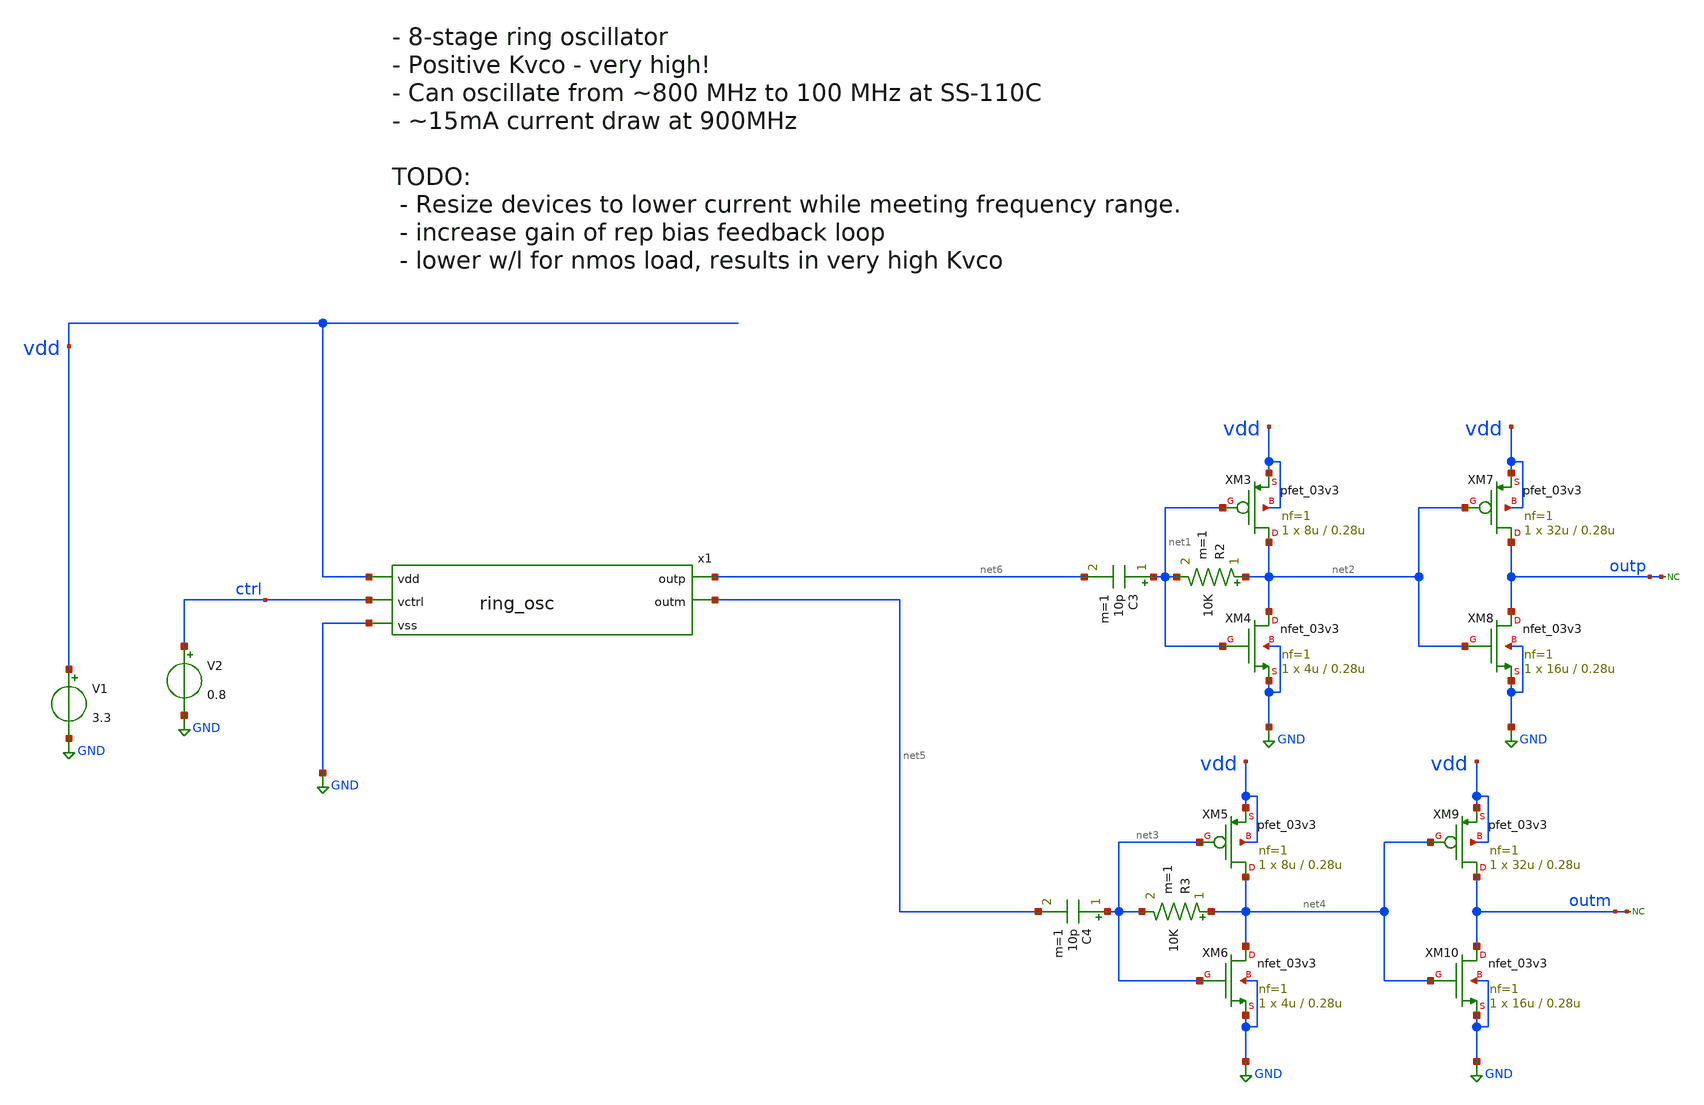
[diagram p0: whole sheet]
** sch_path: xschem/tb_ring_osc_p.sch
**.subckt tb_ring_osc_p
V1 vdd GND 3.3
x1 net6 net5 vdd ctrl GND ring_osc
V2 ctrl GND 0.8
XM3 net2 net1 vdd vdd pfet_03v3 L=0.28u W=8u nf=1 ad='int((nf+1)/2) * W/nf * 0.18u' as='int((nf+2)/2) * W/nf * 0.18u'
+ pd='2*int((nf+1)/2) * (W/nf + 0.18u)' ps='2*int((nf+2)/2) * (W/nf + 0.18u)' nrd='0.18u / W' nrs='0.18u / W'
+ sa=0 sb=0 sd=0 m=1
XM4 net2 net1 GND GND nfet_03v3 L=0.28u W=4u nf=1 ad='int((nf+1)/2) * W/nf * 0.18u' as='int((nf+2)/2) * W/nf * 0.18u'
+ pd='2*int((nf+1)/2) * (W/nf + 0.18u)' ps='2*int((nf+2)/2) * (W/nf + 0.18u)' nrd='0.18u / W' nrs='0.18u / W'
+ sa=0 sb=0 sd=0 m=1
R2 net2 net1 10K m=1
C3 net1 net6 10p m=1
XM5 net4 net3 vdd vdd pfet_03v3 L=0.28u W=8u nf=1 ad='int((nf+1)/2) * W/nf * 0.18u' as='int((nf+2)/2) * W/nf * 0.18u'
+ pd='2*int((nf+1)/2) * (W/nf + 0.18u)' ps='2*int((nf+2)/2) * (W/nf + 0.18u)' nrd='0.18u / W' nrs='0.18u / W'
+ sa=0 sb=0 sd=0 m=1
XM6 net4 net3 GND GND nfet_03v3 L=0.28u W=4u nf=1 ad='int((nf+1)/2) * W/nf * 0.18u' as='int((nf+2)/2) * W/nf * 0.18u'
+ pd='2*int((nf+1)/2) * (W/nf + 0.18u)' ps='2*int((nf+2)/2) * (W/nf + 0.18u)' nrd='0.18u / W' nrs='0.18u / W'
+ sa=0 sb=0 sd=0 m=1
R3 net4 net3 10K m=1
C4 net3 net5 10p m=1
* noconn outp
XM7 outp net2 vdd vdd pfet_03v3 L=0.28u W=32u nf=1 ad='int((nf+1)/2) * W/nf * 0.18u' as='int((nf+2)/2) * W/nf * 0.18u'
+ pd='2*int((nf+1)/2) * (W/nf + 0.18u)' ps='2*int((nf+2)/2) * (W/nf + 0.18u)' nrd='0.18u / W' nrs='0.18u / W'
+ sa=0 sb=0 sd=0 m=1
XM8 outp net2 GND GND nfet_03v3 L=0.28u W=16u nf=1 ad='int((nf+1)/2) * W/nf * 0.18u' as='int((nf+2)/2) * W/nf * 0.18u'
+ pd='2*int((nf+1)/2) * (W/nf + 0.18u)' ps='2*int((nf+2)/2) * (W/nf + 0.18u)' nrd='0.18u / W' nrs='0.18u / W'
+ sa=0 sb=0 sd=0 m=1
XM9 outm net4 vdd vdd pfet_03v3 L=0.28u W=32u nf=1 ad='int((nf+1)/2) * W/nf * 0.18u' as='int((nf+2)/2) * W/nf * 0.18u'
+ pd='2*int((nf+1)/2) * (W/nf + 0.18u)' ps='2*int((nf+2)/2) * (W/nf + 0.18u)' nrd='0.18u / W' nrs='0.18u / W'
+ sa=0 sb=0 sd=0 m=1
XM10 outm net4 GND GND nfet_03v3 L=0.28u W=16u nf=1 ad='int((nf+1)/2) * W/nf * 0.18u' as='int((nf+2)/2) * W/nf * 0.18u'
+ pd='2*int((nf+1)/2) * (W/nf + 0.18u)' ps='2*int((nf+2)/2) * (W/nf + 0.18u)' nrd='0.18u / W' nrs='0.18u / W'
+ sa=0 sb=0 sd=0 m=1
* noconn outm
**** begin user architecture code


.include /usr/local/share/pdk/gf180mcuD/libs.tech/ngspice/design.ngspice
.lib /usr/local/share/pdk/gf180mcuD/libs.tech/ngspice/sm141064.ngspice ff
.option temp=-20

.tran 50p 200n

.control
save all

let vc = 0.3
set vctrl_step = 0.15
set vctrl_numsteps = 22
let loopindex = 0
let freq_list = vector($vctrl_numsteps)
let vctrl_list = vector($vctrl_numsteps)

dowhile loopindex < $vctrl_numsteps
  alter V2 = $&vc
  echo $&loopindex
  echo $&vc
  tran 20p 140n
  meas tran tstart when outp=1.65 TD=100n RISE=1
  meas tran tend when outp=1.65 TD=100n RISE=2
  let freq = 1 / ($&tend - $&tstart)
  echo $&freq
  let freq_list[$&loopindex] = freq
  let vctrl_list[$&loopindex] = vc
  let vc = vc + $vctrl_step
  let loopindex = loopindex + 1
end

plot freq_list vs vctrl_list
plot v(outp) v(ctrl)
plot i(V1)
.endc


**** end user architecture code
**.ends
.GLOBAL GND
.end
